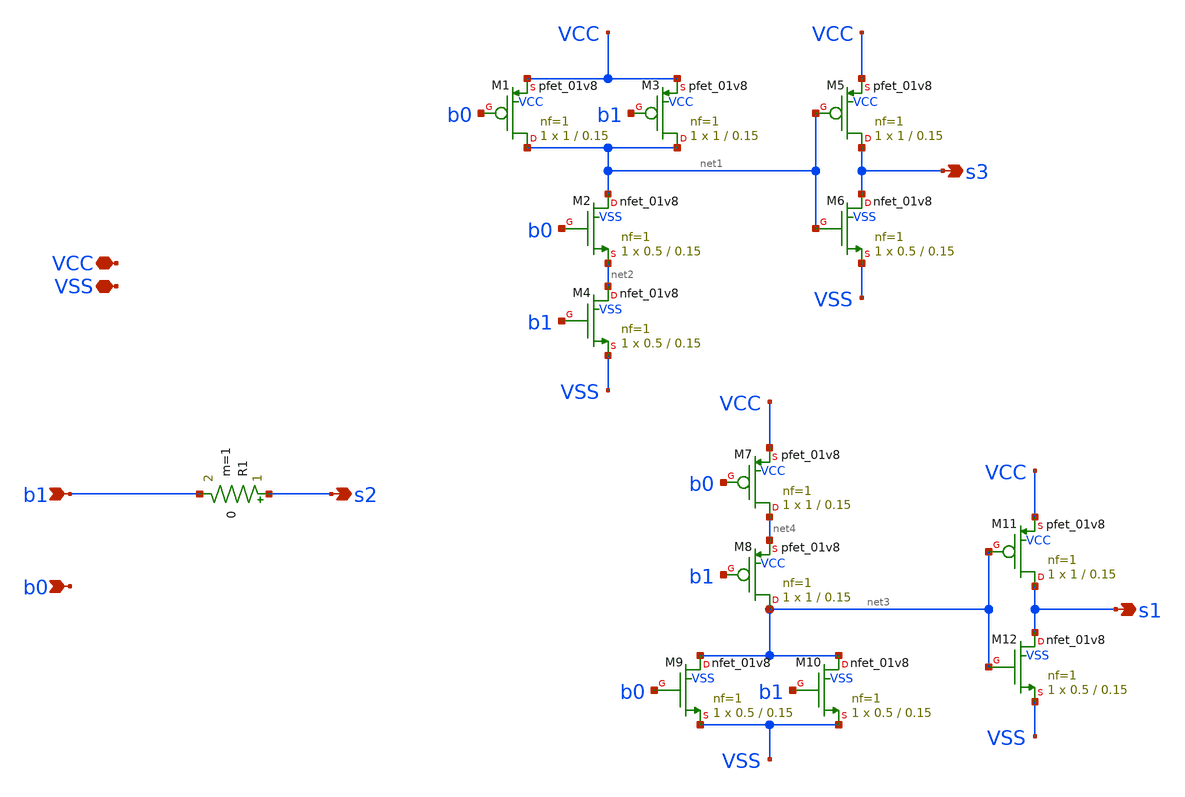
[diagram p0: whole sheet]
** sch_path: xschem/thermo2bit.sch
**.subckt thermo2bit b1 s2 b0 s3 VCC VSS s1
*.ipin b1
*.opin s2
*.ipin b0
*.opin s3
*.iopin VCC
*.iopin VSS
*.opin s1
R1 s2 b1 0 m=1
XM1 net1 b0 VCC VCC sky130_fd_pr__pfet_01v8 L=0.15 W=1 nf=1 ad='int((nf+1)/2) * W/nf * 0.29' as='int((nf+2)/2) * W/nf * 0.29'
+ pd='2*int((nf+1)/2) * (W/nf + 0.29)' ps='2*int((nf+2)/2) * (W/nf + 0.29)' nrd='0.29 / W' nrs='0.29 / W'
+ sa=0 sb=0 sd=0 mult=1 m=1
XM2 net1 b0 net2 VSS sky130_fd_pr__nfet_01v8 L=0.15 W=0.5 nf=1 ad='int((nf+1)/2) * W/nf * 0.29' as='int((nf+2)/2) * W/nf * 0.29'
+ pd='2*int((nf+1)/2) * (W/nf + 0.29)' ps='2*int((nf+2)/2) * (W/nf + 0.29)' nrd='0.29 / W' nrs='0.29 / W'
+ sa=0 sb=0 sd=0 mult=1 m=1
XM3 net1 b1 VCC VCC sky130_fd_pr__pfet_01v8 L=0.15 W=1 nf=1 ad='int((nf+1)/2) * W/nf * 0.29' as='int((nf+2)/2) * W/nf * 0.29'
+ pd='2*int((nf+1)/2) * (W/nf + 0.29)' ps='2*int((nf+2)/2) * (W/nf + 0.29)' nrd='0.29 / W' nrs='0.29 / W'
+ sa=0 sb=0 sd=0 mult=1 m=1
XM4 net2 b1 VSS VSS sky130_fd_pr__nfet_01v8 L=0.15 W=0.5 nf=1 ad='int((nf+1)/2) * W/nf * 0.29' as='int((nf+2)/2) * W/nf * 0.29'
+ pd='2*int((nf+1)/2) * (W/nf + 0.29)' ps='2*int((nf+2)/2) * (W/nf + 0.29)' nrd='0.29 / W' nrs='0.29 / W'
+ sa=0 sb=0 sd=0 mult=1 m=1
XM5 s3 net1 VCC VCC sky130_fd_pr__pfet_01v8 L=0.15 W=1 nf=1 ad='int((nf+1)/2) * W/nf * 0.29' as='int((nf+2)/2) * W/nf * 0.29'
+ pd='2*int((nf+1)/2) * (W/nf + 0.29)' ps='2*int((nf+2)/2) * (W/nf + 0.29)' nrd='0.29 / W' nrs='0.29 / W'
+ sa=0 sb=0 sd=0 mult=1 m=1
XM6 s3 net1 VSS VSS sky130_fd_pr__nfet_01v8 L=0.15 W=0.5 nf=1 ad='int((nf+1)/2) * W/nf * 0.29' as='int((nf+2)/2) * W/nf * 0.29'
+ pd='2*int((nf+1)/2) * (W/nf + 0.29)' ps='2*int((nf+2)/2) * (W/nf + 0.29)' nrd='0.29 / W' nrs='0.29 / W'
+ sa=0 sb=0 sd=0 mult=1 m=1
XM11 s1 net3 VCC VCC sky130_fd_pr__pfet_01v8 L=0.15 W=1 nf=1 ad='int((nf+1)/2) * W/nf * 0.29' as='int((nf+2)/2) * W/nf * 0.29'
+ pd='2*int((nf+1)/2) * (W/nf + 0.29)' ps='2*int((nf+2)/2) * (W/nf + 0.29)' nrd='0.29 / W' nrs='0.29 / W'
+ sa=0 sb=0 sd=0 mult=1 m=1
XM12 s1 net3 VSS VSS sky130_fd_pr__nfet_01v8 L=0.15 W=0.5 nf=1 ad='int((nf+1)/2) * W/nf * 0.29' as='int((nf+2)/2) * W/nf * 0.29'
+ pd='2*int((nf+1)/2) * (W/nf + 0.29)' ps='2*int((nf+2)/2) * (W/nf + 0.29)' nrd='0.29 / W' nrs='0.29 / W'
+ sa=0 sb=0 sd=0 mult=1 m=1
XM7 net4 b0 VCC VCC sky130_fd_pr__pfet_01v8 L=0.15 W=1 nf=1 ad='int((nf+1)/2) * W/nf * 0.29' as='int((nf+2)/2) * W/nf * 0.29'
+ pd='2*int((nf+1)/2) * (W/nf + 0.29)' ps='2*int((nf+2)/2) * (W/nf + 0.29)' nrd='0.29 / W' nrs='0.29 / W'
+ sa=0 sb=0 sd=0 mult=1 m=1
XM8 net3 b1 net4 VCC sky130_fd_pr__pfet_01v8 L=0.15 W=1 nf=1 ad='int((nf+1)/2) * W/nf * 0.29' as='int((nf+2)/2) * W/nf * 0.29'
+ pd='2*int((nf+1)/2) * (W/nf + 0.29)' ps='2*int((nf+2)/2) * (W/nf + 0.29)' nrd='0.29 / W' nrs='0.29 / W'
+ sa=0 sb=0 sd=0 mult=1 m=1
XM9 net3 b0 VSS VSS sky130_fd_pr__nfet_01v8 L=0.15 W=0.5 nf=1 ad='int((nf+1)/2) * W/nf * 0.29' as='int((nf+2)/2) * W/nf * 0.29'
+ pd='2*int((nf+1)/2) * (W/nf + 0.29)' ps='2*int((nf+2)/2) * (W/nf + 0.29)' nrd='0.29 / W' nrs='0.29 / W'
+ sa=0 sb=0 sd=0 mult=1 m=1
XM10 net3 b1 VSS VSS sky130_fd_pr__nfet_01v8 L=0.15 W=0.5 nf=1 ad='int((nf+1)/2) * W/nf * 0.29' as='int((nf+2)/2) * W/nf * 0.29'
+ pd='2*int((nf+1)/2) * (W/nf + 0.29)' ps='2*int((nf+2)/2) * (W/nf + 0.29)' nrd='0.29 / W' nrs='0.29 / W'
+ sa=0 sb=0 sd=0 mult=1 m=1
**.ends
.end
